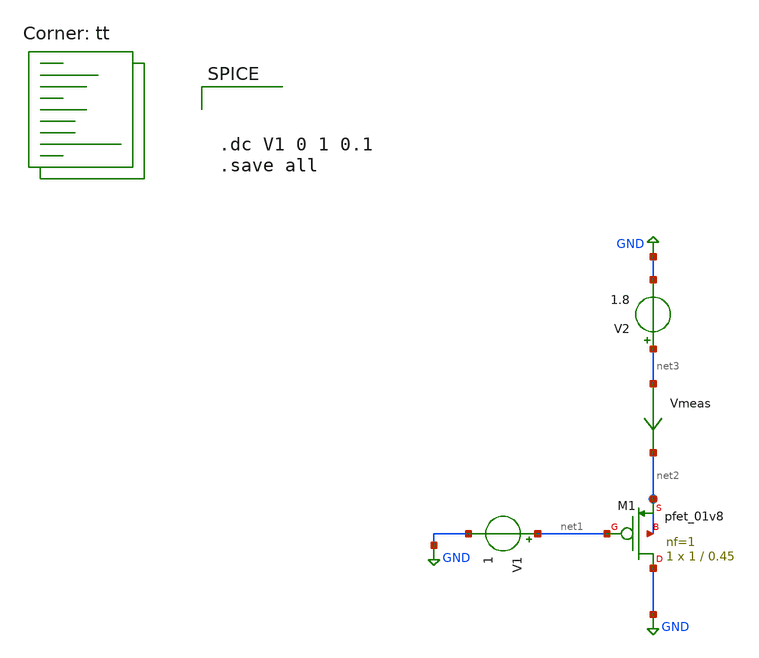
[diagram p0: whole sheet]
** sch_path: userLib/NMOSparam.sch
**.subckt NMOSparam
Vmeas net3 net2 0
.save i(vmeas)
V1 net1 GND 1
V2 net3 GND 1.8
XM1 GND net1 net2 net2 sky130_fd_pr__pfet_01v8 L=0.45 W=1 nf=1 ad='int((nf+1)/2) * W/nf * 0.29' as='int((nf+2)/2) * W/nf * 0.29'
+ pd='2*int((nf+1)/2) * (W/nf + 0.29)' ps='2*int((nf+2)/2) * (W/nf + 0.29)' nrd='0.29 / W' nrs='0.29 / W'
+ sa=0 sb=0 sd=0 mult=1 m=1
**** begin user architecture code



.dc V1 0 1 0.1
.save all


.lib $::SKYWATER_MODELS/sky130.lib.spice tt
**** end user architecture code
**.ends
.GLOBAL GND
.end
